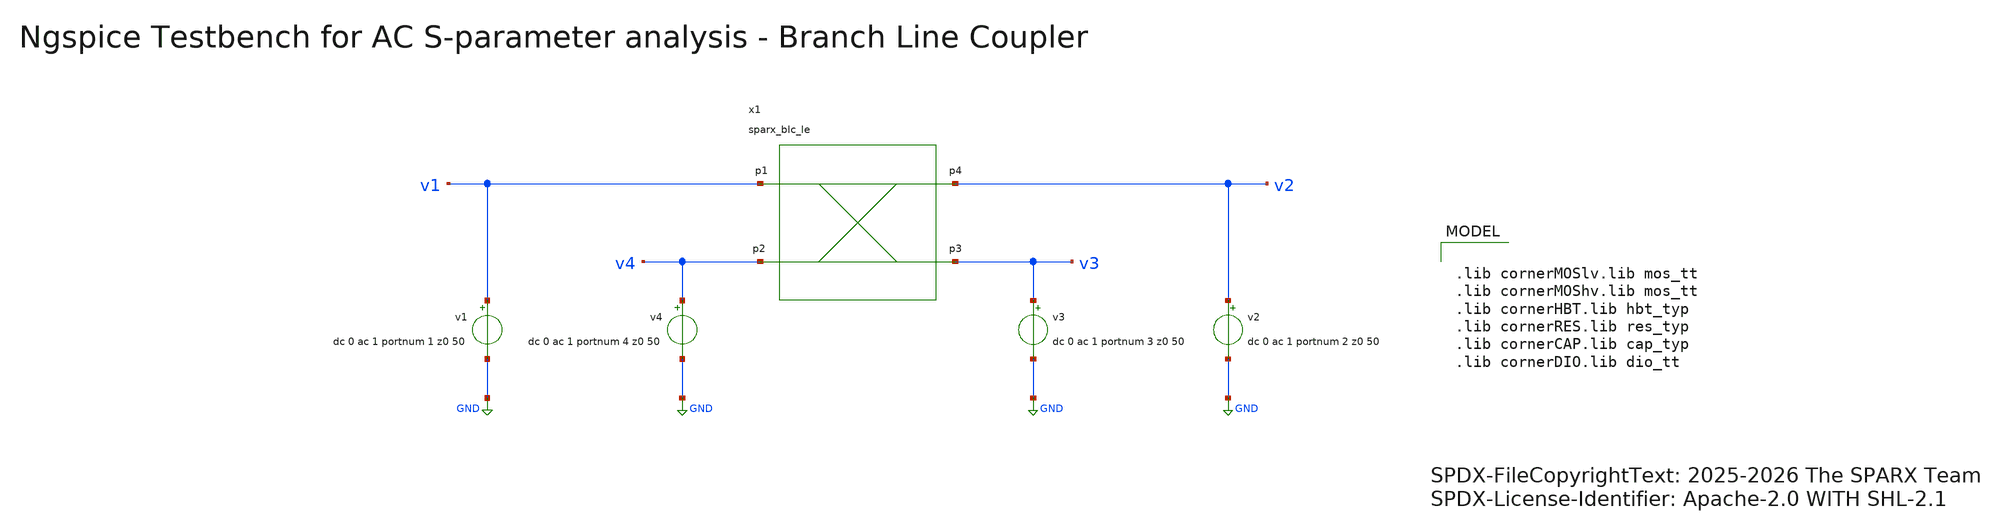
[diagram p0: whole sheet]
** sch_path: testbenches/xschem/sparx_blc_le_tb_acsp_ngspice.sch
* SPDX-FileCopyrightText: 2025-2026 The SPARX Team
* SPDX-License-Identifier: Apache-2.0 WITH SHL-2.1
**.subckt sparx_blc_le_tb_acsp_ngspice
v2 v2 GND dc 0 ac 1 portnum 2 z0 50
v3 v3 GND dc 0 ac 1 portnum 3 z0 50
v4 v4 GND dc 0 ac 1 portnum 4 z0 50
v1 v1 GND dc 0 ac 1 portnum 1 z0 50
x1 v1 v4 v3 v2 sparx_blc_le
**** begin user architecture code


.include ../../../netlist/spice/sparx_blc_le.spice
.include ../sim_range.spice
.param temp=27
.options savecurrents klu method=gear reltol=1e-3 abstol=1e-15 gmin=1e-15
.control

save all

set wr_vecnames
set wr_singlescale

* User Constants
* f_min / f_max come from ../sim_range.spice (.csparam),
* auto-synced to the loaded Touchstone by snp2le.
* edit that file for a standalone run.

* Operating Point Analysis
op
remzerovec
write @schname\.raw
set appendwrite

* AC S-Parameter Analysis
sp lin 1001 $&const.f_min $&const.f_max
remzerovec
write @schname\.raw
set appendwrite

* Calculating S-Parameters
let s11_dB = db(S_1_1)
let s21_dB = db(S_2_1)
let s12_dB = db(S_1_2)
let s22_dB = db(S_2_2)
let s33_dB = db(s_3_3)
let s31_dB = db(S_3_1)
let s13_dB = db(S_1_3)
let s32_dB = db(S_3_2)
let s23_dB = db(S_2_3)
let s44_dB = db(S_4_4)
let s41_dB = db(S_4_1)
let s14_dB = db(S_1_4)
let s42_dB = db(S_4_2)
let s24_dB = db(S_2_4)
let s43_dB = db(s_4_3)
let s34_dB = db(s_3_4)

let s11_deg = cph(S_1_1) * 180/pi
let s21_deg = cph(S_2_1) * 180/pi
let s12_deg = cph(S_1_2) * 180/pi
let s22_deg = cph(S_2_2) * 180/pi
let s33_deg = cph(s_3_3) * 180/pi
let s31_deg = cph(S_3_1) * 180/pi
let s13_deg = cph(S_1_3) * 180/pi
let s32_deg = cph(S_3_2) * 180/pi
let s23_deg = cph(S_2_3) * 180/pi
let s44_deg = cph(s_4_4) * 180/pi
let s41_deg = cph(S_4_1) * 180/pi
let s14_deg = cph(S_1_4) * 180/pi
let s42_deg = cph(S_4_2) * 180/pi
let s24_deg = cph(S_2_4) * 180/pi
let s43_deg = cph(S_4_3) * 180/pi
let s34_deg = cph(S_3_4) * 180/pi

* Plotting
plot s11_dB s22_dB s33_dB s44_dB
plot s11_deg s22_deg s33_deg s44_deg
plot s12_dB s21_dB s13_dB s31_dB s14_dB s41_dB
plot s12_deg s21_deg s13_deg s31_deg s14_deg s41_deg
plot s23_dB s32_dB s24_dB s42_dB
plot s23_deg s32_deg s24_deg s42_deg
plot s34_dB s43_dB
plot s34_deg s43_deg

* Write Data
unset appendwrite
set wr_vecnames
set wr_singlescale
wrdata ../plot_simulations/data/@schname\.txt  s11_dB s22_dB s33_dB s44_dB  s11_deg s22_deg s33_deg
+ s44_deg  s12_dB s21_dB s13_dB s31_dB s14_dB s41_dB  s12_deg s21_deg s13_deg s31_deg s14_deg s41_deg  s23_dB
+ s32_dB s24_dB s42_dB  s23_deg s32_deg s24_deg s42_deg  s34_dB s43_dB  s34_deg s43_deg

*quit
.endc



.lib cornerMOSlv.lib mos_tt
.lib cornerMOShv.lib mos_tt
.lib cornerHBT.lib hbt_typ
.lib cornerRES.lib res_typ
.lib cornerCAP.lib cap_typ
.lib cornerDIO.lib dio_tt

**** end user architecture code
**.ends
.GLOBAL GND
.end
